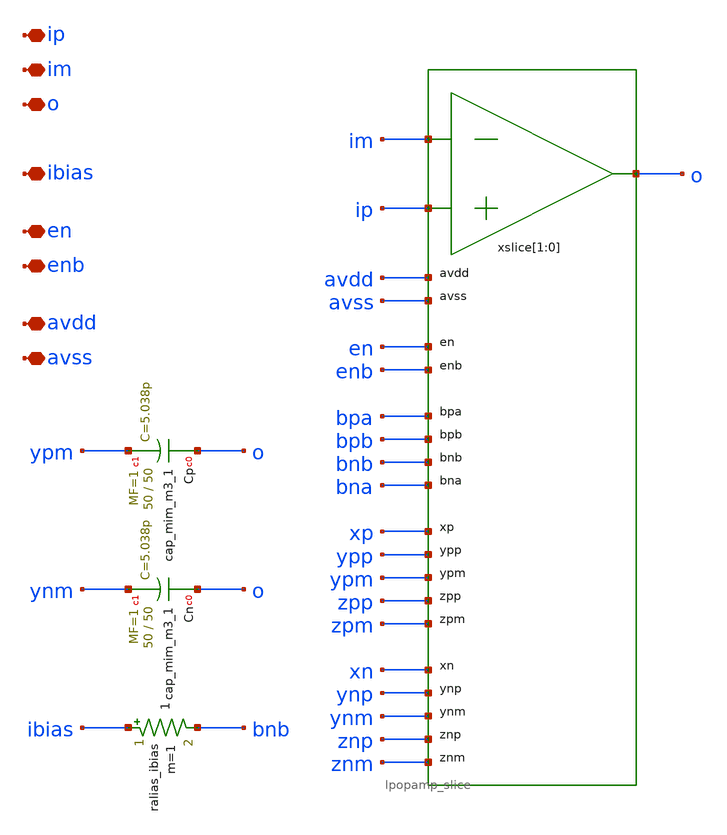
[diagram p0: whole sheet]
** sch_path: xschem/lpopampb.sch
**.subckt lpopampb avdd avss ip im o ibias en enb
*.iopin avdd
*.iopin avss
*.iopin ip
*.iopin im
*.iopin o
*.iopin ibias
*.iopin en
*.iopin enb
xslice[1] im ip o avdd avss en enb bpa bpb bnb bna xp ypp ypm zpp zpm xn ynp ynm znp znm
+ lpopamp_slice
xslice[0] im ip o avdd avss en enb bpa bpb bnb bna xp ypp ypm zpp zpm xn ynp ynm znp znm
+ lpopamp_slice
ralias_ibias ibias bnb 1 m=1
XCp o ypm sky130_fd_pr__cap_mim_m3_1 W=50 L=50 MF=1 m=1
XCn o ynm sky130_fd_pr__cap_mim_m3_1 W=50 L=50 MF=1 m=1
**.ends
.end
